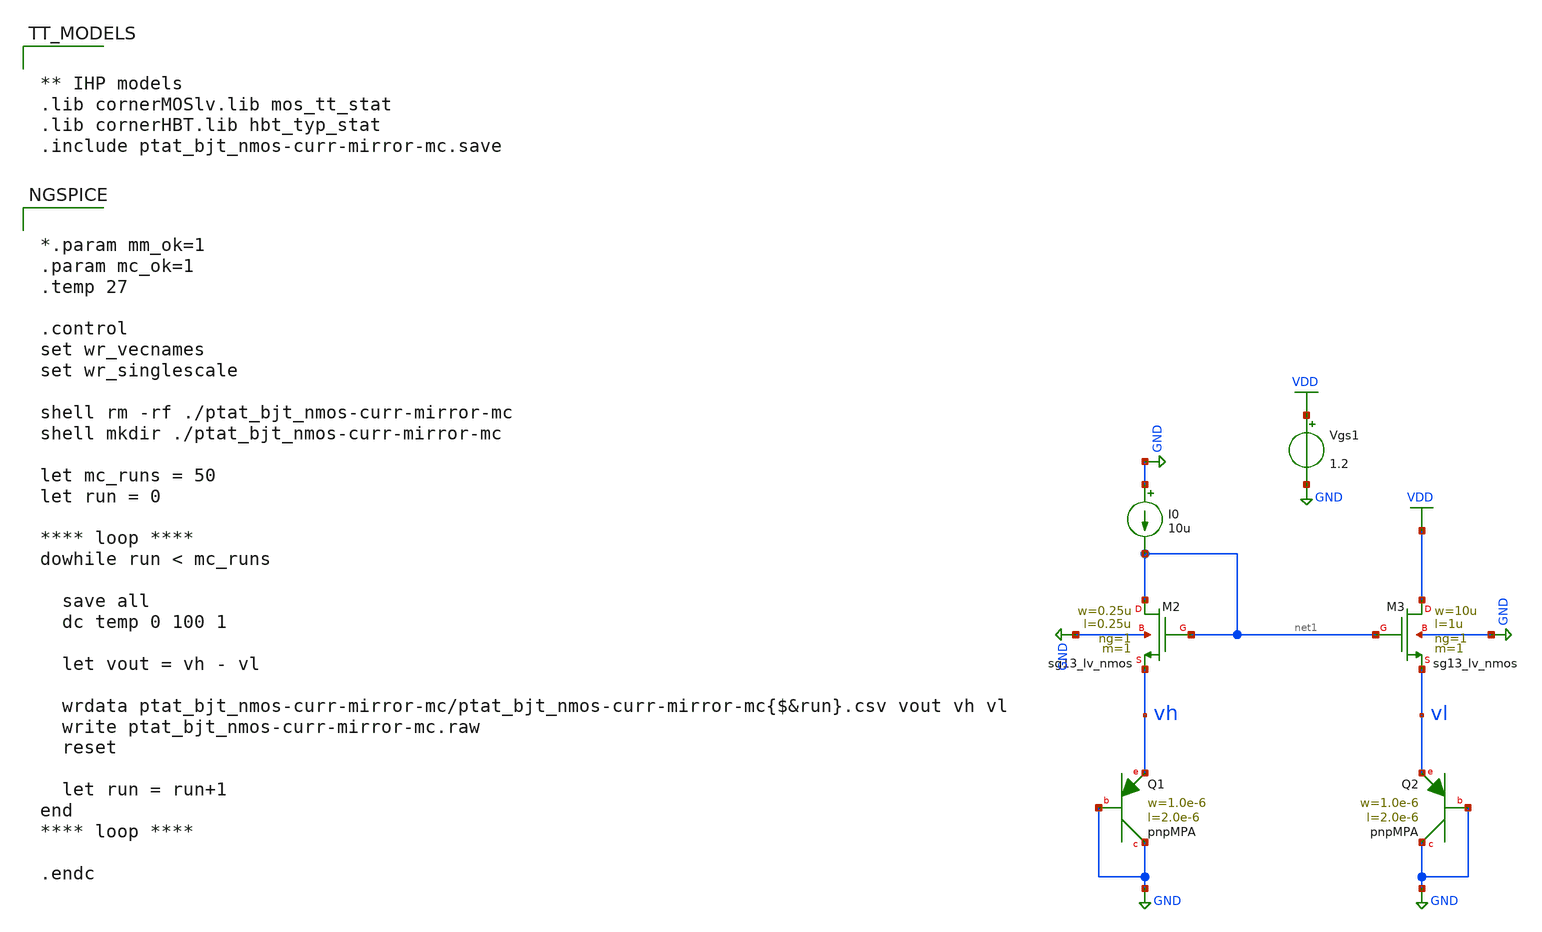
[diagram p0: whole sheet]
** sch_path: TempSensor/design_data/xschem/ptat_bjt_nmos-curr-mirror-mc.sch
**.subckt ptat_bjt_nmos-curr-mirror-mc
XM2 net1 net1 vh GND sg13_lv_nmos w=0.25u l=0.25u ng=1 m=1 mm_ok=1
XM3 VDD net1 vl GND sg13_lv_nmos w=10u l=1u ng=1 m=1 mm_ok=1
I0 GND net1 10u
Vgs1 VDD GND 1.2
XQ2 GND GND vl pnpMPA a=2p p=6u m=1
XQ1 GND GND vh pnpMPA a=2p p=6u m=1
**** begin user architecture code


*.param mm_ok=1
.param mc_ok=1
.temp 27

.control
set wr_vecnames
set wr_singlescale

shell rm -rf ./ptat_bjt_nmos-curr-mirror-mc
shell mkdir ./ptat_bjt_nmos-curr-mirror-mc

let mc_runs = 50
let run = 0

**** loop ****
dowhile run < mc_runs

  save all
  dc temp 0 100 1

  let vout = vh - vl

  wrdata ptat_bjt_nmos-curr-mirror-mc/ptat_bjt_nmos-curr-mirror-mc{$&run}.csv vout vh vl
  write ptat_bjt_nmos-curr-mirror-mc.raw
  reset

  let run = run+1
end
**** loop ****

.endc




** IHP models
.lib cornerMOSlv.lib mos_tt_stat
.lib cornerHBT.lib hbt_typ_stat
.include ptat_bjt_nmos-curr-mirror-mc.save


**** end user architecture code
**.ends
.GLOBAL GND
.GLOBAL VDD
.end
